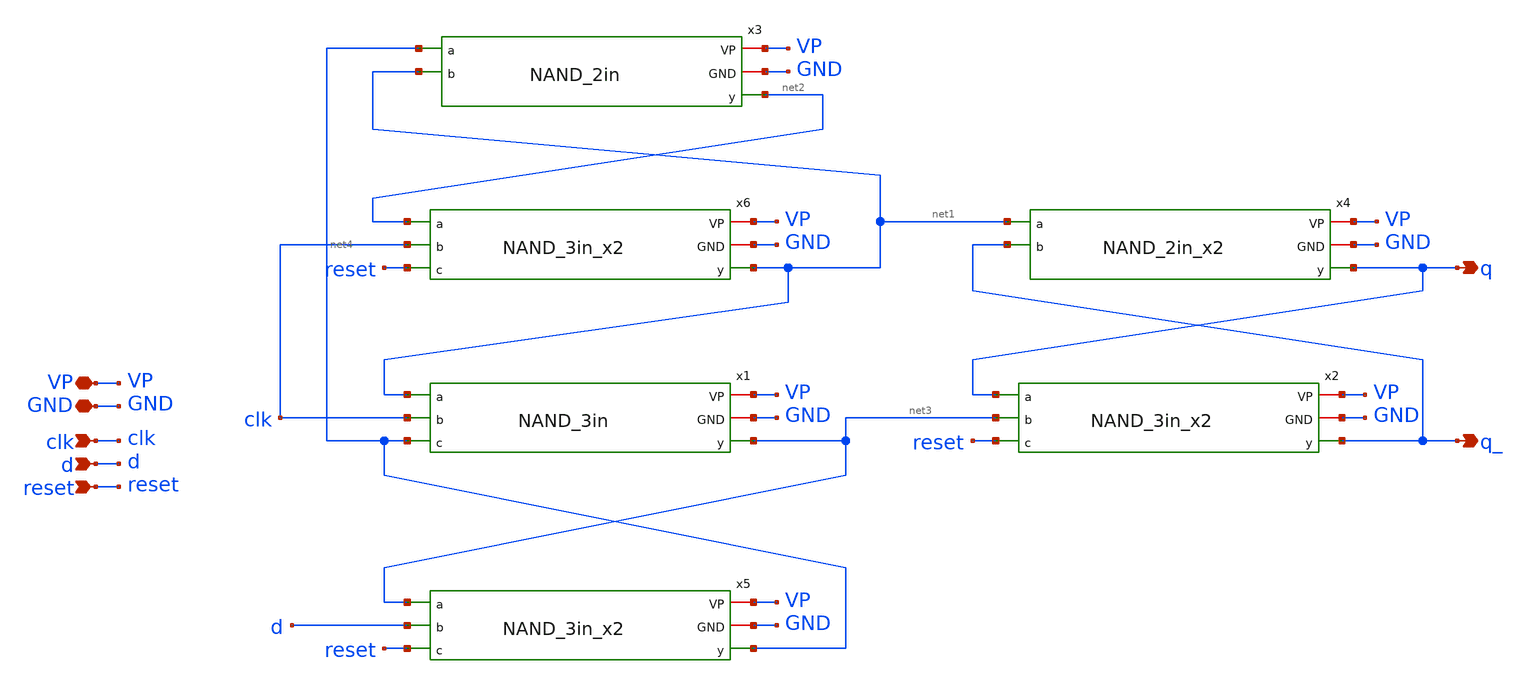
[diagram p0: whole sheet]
** sch_path: schematics/divider/schematics/d_flip_flop_reset.sch
**.subckt d_flip_flop_reset GND clk VP d q q_ reset
*.iopin GND
*.ipin clk
*.iopin VP
*.ipin d
*.opin q
*.opin q_
*.ipin reset
x3 VP GND net4 net2 net1 NAND_2in
x2 VP GND q q_ net3 reset NAND_3in_x2
x5 VP GND net3 net4 d reset NAND_3in_x2
x6 VP GND net2 net1 clk reset NAND_3in_x2
x4 VP GND net1 q q_ NAND_2in_x2
x1 VP GND net1 net3 clk net4 NAND_3in
**.ends

* expanding   symbol:  /foss/designs/CHIP-PLL/schematics/divider/schematics/NAND_2in.sym # of pins=5
** sym_path: schematics/divider/schematics/NAND_2in.sym
** sch_path: schematics/divider/schematics/NAND_2in.sch
.subckt NAND_2in VP GND a y b
*.opin y
*.iopin GND
*.ipin a
*.iopin VP
*.ipin b
XM1 y a net1 GND sg13_lv_nmos w=0.15u l=0.13u ng=1 m=1 mm_ok=1
XM3 net1 b GND GND sg13_lv_nmos w=0.15u l=0.13u ng=1 m=1 mm_ok=1
XM2 y b VP VP sg13_lv_pmos w=0.15u l=0.13u ng=1 m=1 mm_ok=1
XM4 y a VP VP sg13_lv_pmos w=0.15u l=0.13u ng=1 m=1 mm_ok=1
.ends


* expanding   symbol:  /foss/designs/CHIP-PLL/schematics/divider/schematics/NAND_3in_x2.sym # of
*+ pins=6
** sym_path: schematics/divider/schematics/NAND_3in_x2.sym
** sch_path: schematics/divider/schematics/NAND_3in_x2.sch
.subckt NAND_3in_x2 VP GND a y b c
*.opin y
*.iopin GND
*.ipin a
*.iopin VP
*.ipin b
*.ipin c
XM1 y a net2 GND sg13_lv_nmos w=0.150u l=0.13u ng=1 m=8 mm_ok=1
XM3 net2 b net1 GND sg13_lv_nmos w=0.150u l=0.13u ng=1 m=8 mm_ok=1
XM4 net1 c GND GND sg13_lv_nmos w=0.150u l=0.13u ng=1 m=8 mm_ok=1
XM7 y c VP VP sg13_lv_pmos w=0.150u l=0.13u ng=1 m=2 mm_ok=1
XM2 y a VP VP sg13_lv_pmos w=0.150u l=0.13u ng=1 m=2 mm_ok=1
XM5 y b VP VP sg13_lv_pmos w=0.150u l=0.13u ng=1 m=2 mm_ok=1
.ends


* expanding   symbol:  /foss/designs/CHIP-PLL/schematics/divider/schematics/NAND_2in_x2.sym # of
*+ pins=5
** sym_path: schematics/divider/schematics/NAND_2in_x2.sym
** sch_path: schematics/divider/schematics/NAND_2in_x2.sch
.subckt NAND_2in_x2 VP GND a y b
*.opin y
*.iopin GND
*.ipin a
*.iopin VP
*.ipin b
XM1 y a net1 GND sg13_lv_nmos w=0.6u l=0.13u ng=1 m=1 mm_ok=1
XM2 y b VP VP sg13_lv_pmos w=0.3u l=0.13u ng=1 m=1 mm_ok=1
XM3 net1 b GND GND sg13_lv_nmos w=0.6u l=0.13u ng=1 m=1 mm_ok=1
XM4 y a VP VP sg13_lv_pmos w=0.3u l=0.13u ng=1 m=1 mm_ok=1
.ends


* expanding   symbol:  /foss/designs/CHIP-PLL/schematics/divider/schematics/NAND_3in.sym # of pins=6
** sym_path: schematics/divider/schematics/NAND_3in.sym
** sch_path: schematics/divider/schematics/NAND_3in.sch
.subckt NAND_3in VP GND a y b c
*.opin y
*.iopin GND
*.ipin a
*.iopin VP
*.ipin b
*.ipin c
XM1 y a net2 GND sg13_lv_nmos w=0.15u l=0.13u ng=1 m=1 mm_ok=1
XM3 net2 b net1 GND sg13_lv_nmos w=0.15u l=0.13u ng=1 m=1 mm_ok=1
XM4 net1 c GND GND sg13_lv_nmos w=0.15u l=0.13u ng=1 m=1 mm_ok=1
XM7 y c VP VP sg13_lv_pmos w=0.15u l=0.13u ng=1 m=1 mm_ok=1
XM2 y a VP VP sg13_lv_pmos w=0.15u l=0.13u ng=1 m=1 mm_ok=1
XM5 y b VP VP sg13_lv_pmos w=0.15u l=0.13u ng=1 m=1 mm_ok=1
.ends

.end
